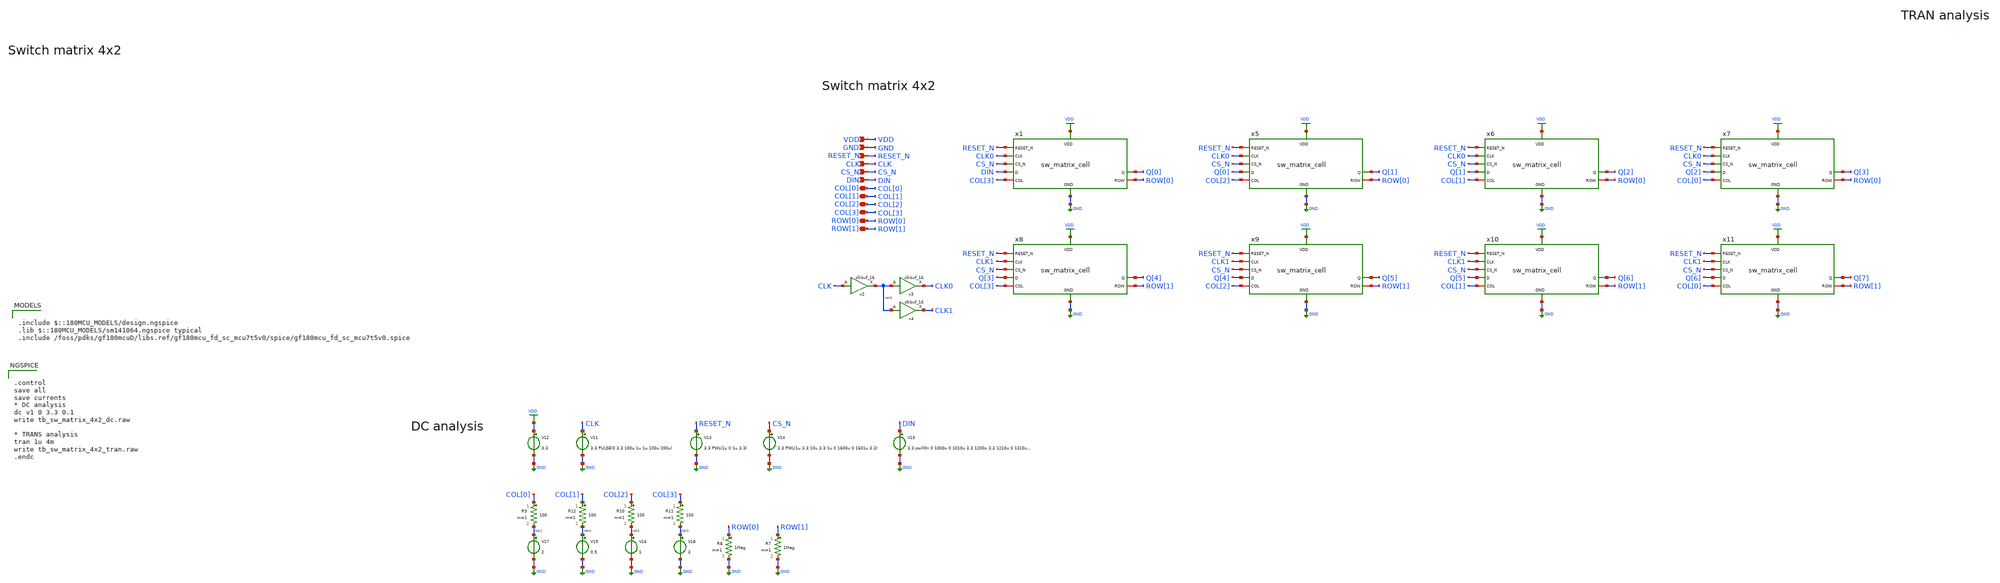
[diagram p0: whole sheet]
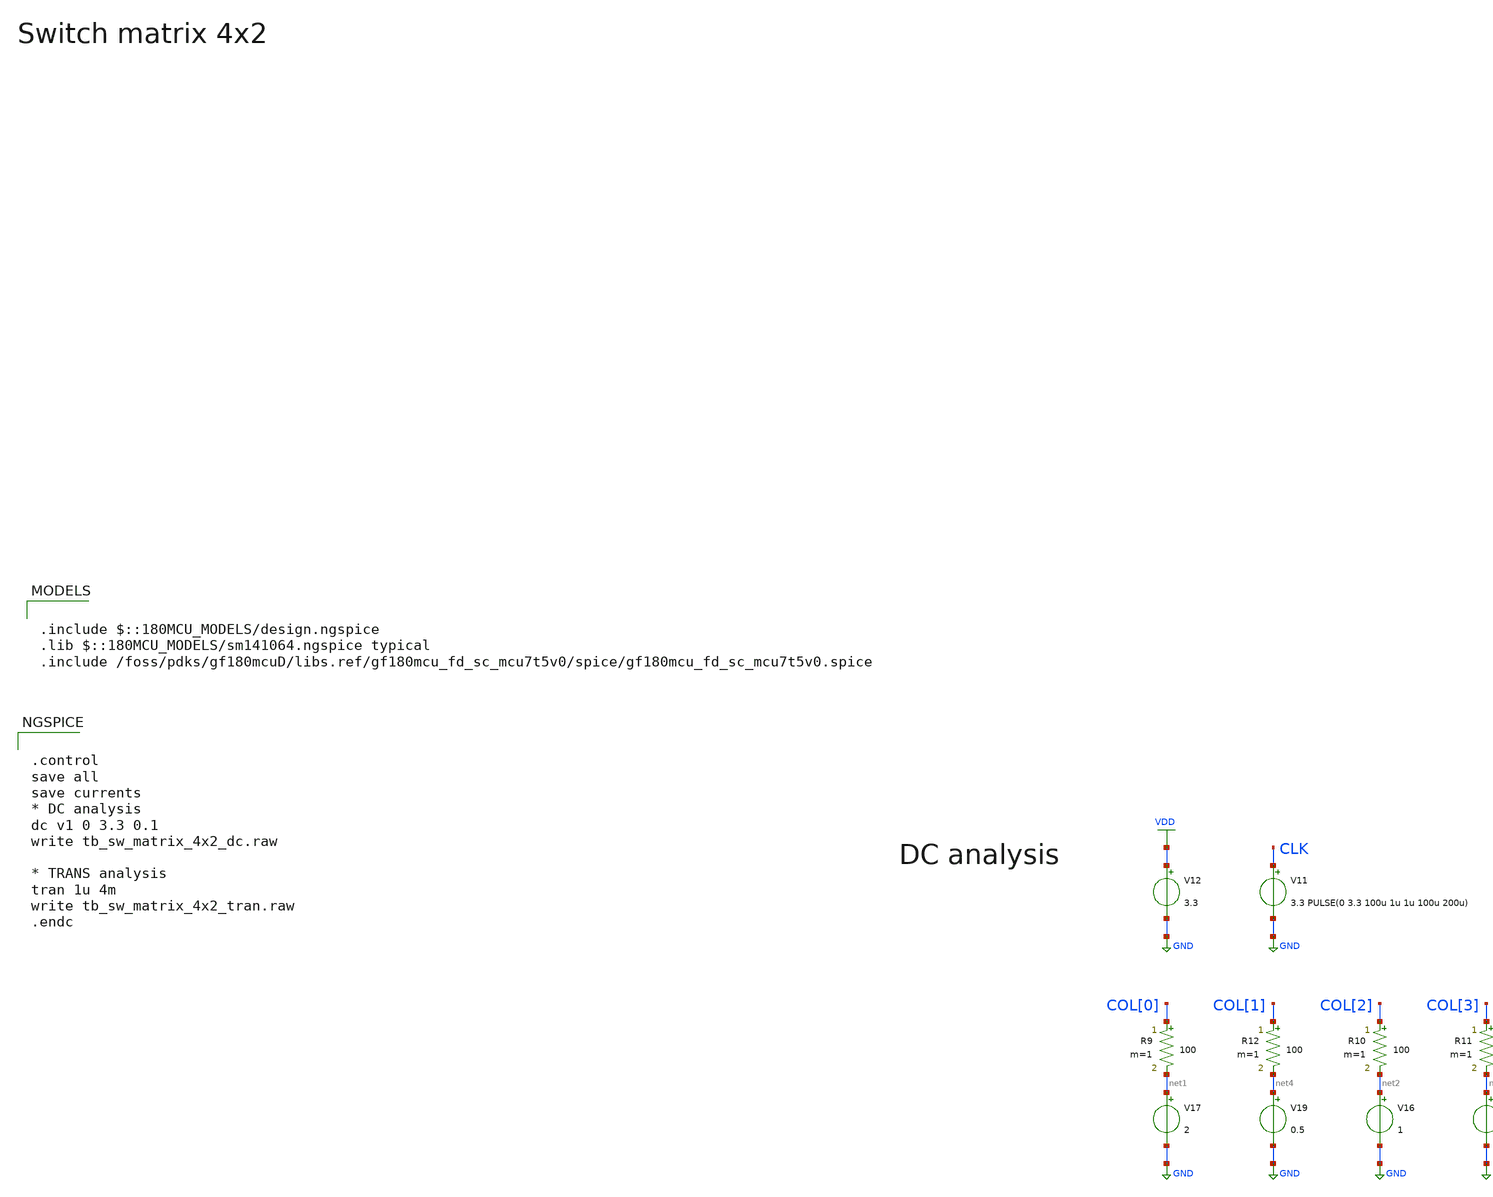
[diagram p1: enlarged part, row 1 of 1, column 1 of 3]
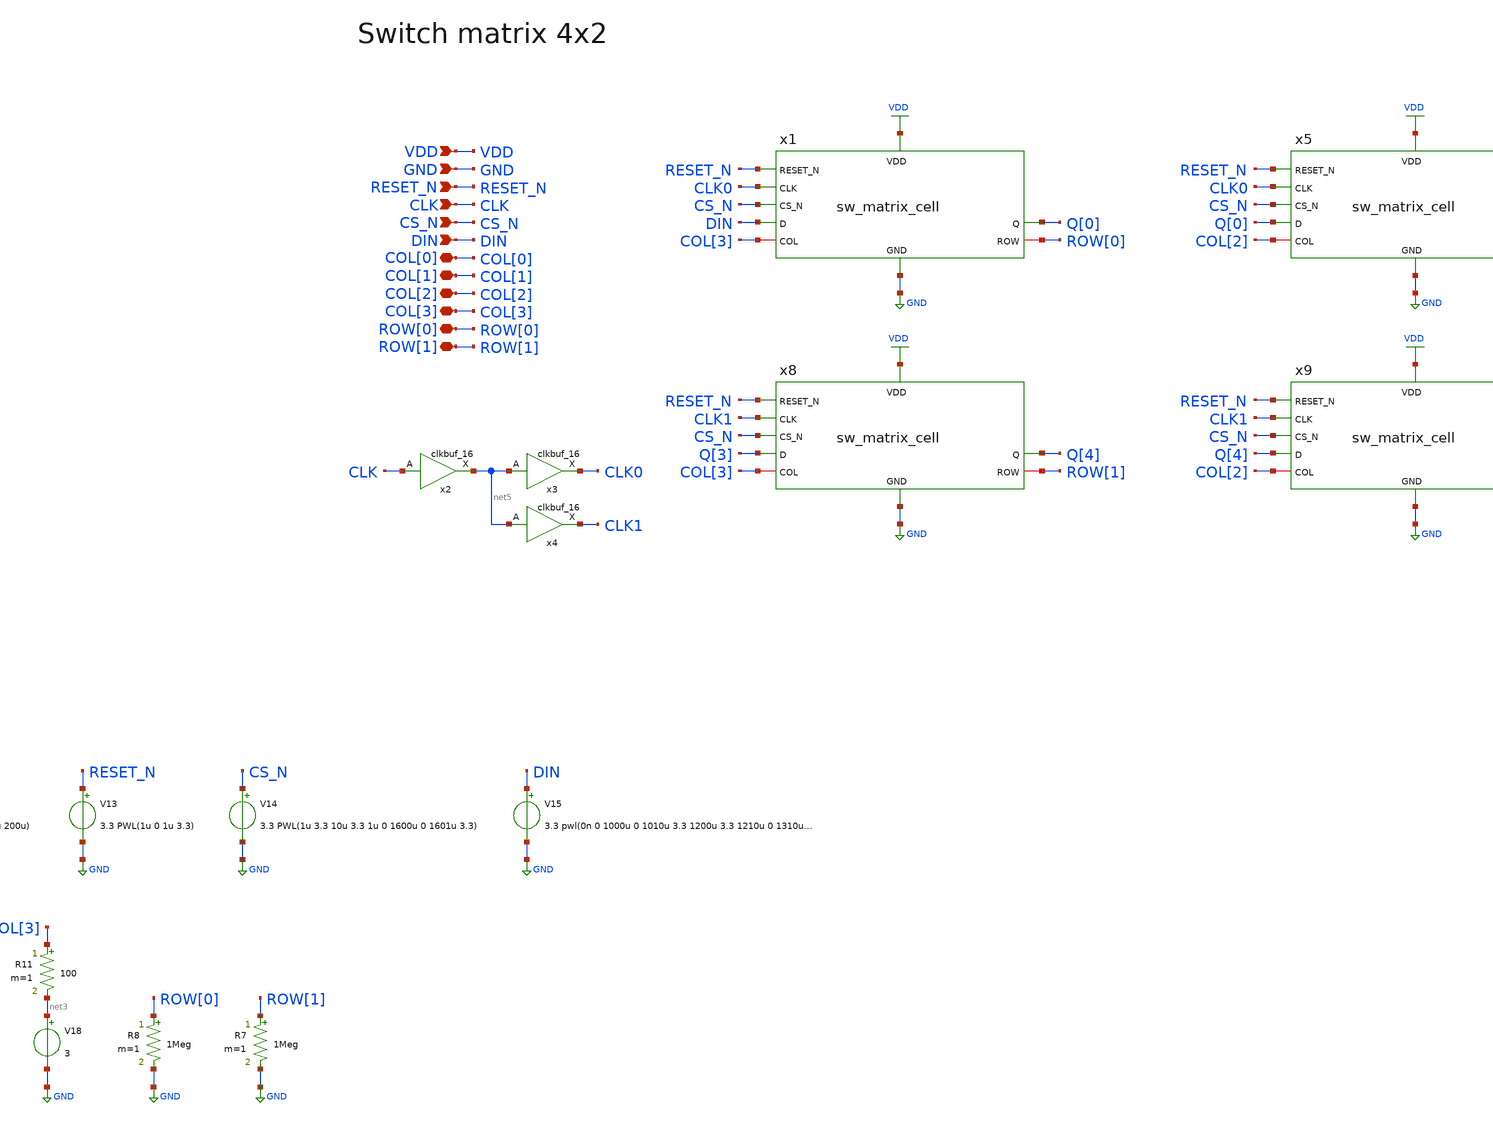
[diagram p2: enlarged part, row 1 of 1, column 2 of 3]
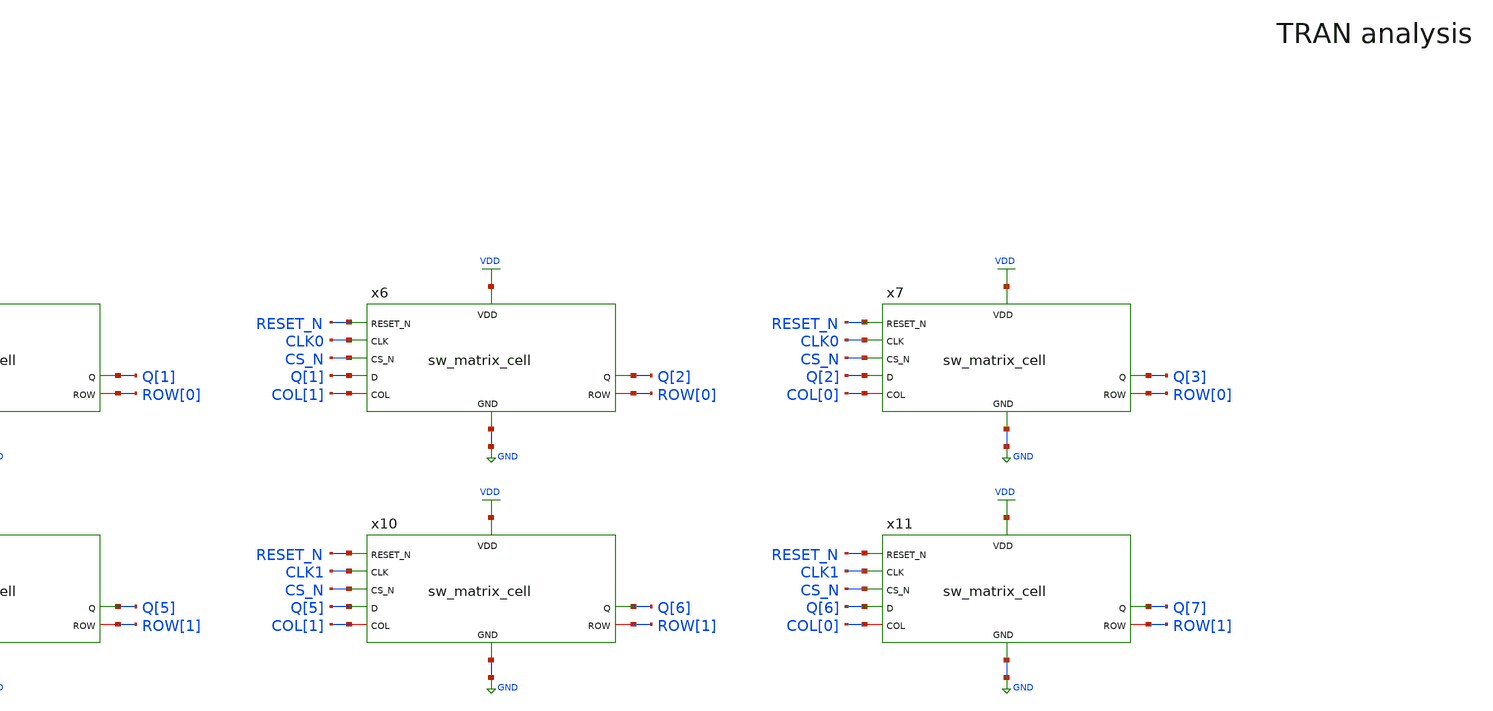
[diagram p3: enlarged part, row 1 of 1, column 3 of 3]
** sch_path: designs/libs/tb_analog/tb_sw_matrix/tb_sw_matrix_4x2.sch
* Copyright 2022 GlobalFoundries PDK Authors
* Licensed under the Apache License, Version 2.0 (the "License");
* you may not use this file except in compliance with the License.
* You may obtain a copy of the License at
* https://www.apache.org/licenses/LICENSE-2.0
* Unless required by applicable law or agreed to in writing, software
* distributed under the License is distributed on an "AS IS" BASIS,
* WITHOUT WARRANTIES OR CONDITIONS OF ANY KIND, either express or implied.
* See the License for the specific language governing permissions and
* limitations under the License.
**.subckt tb_sw_matrix_4x2 VDD GND RESET_N CLK CS_N DIN COL[0] COL[1] COL[2] COL[3] ROW[0] ROW[1]
*.ipin VDD
*.ipin GND
*.ipin RESET_N
*.ipin CLK
*.ipin CS_N
*.ipin DIN
*.iopin COL[0]
*.iopin COL[1]
*.iopin COL[2]
*.iopin COL[3]
*.iopin ROW[0]
*.iopin ROW[1]
V11 CLK GND 3.3 PULSE(0 3.3 100u 1u 1u 100u 200u)
V12 VDD GND 3.3
R7 ROW[1] GND 1Meg m=1
R8 ROW[0] GND 1Meg m=1
V13 RESET_N GND 3.3 PWL(1u 0 1u 3.3)
V14 CS_N GND 3.3 PWL(1u 3.3 10u 3.3 1u 0 1600u 0 1601u 3.3)
V15 DIN GND 3.3 pwl(0n 0 1000u 0 1010u 3.3 1200u 3.3 1210u 0 1310u 0)
R9 COL[0] net1 100 m=1
R10 COL[2] net2 100 m=1
V16 net2 GND 1
V17 net1 GND 2
R11 COL[3] net3 100 m=1
V18 net3 GND 3
R12 COL[1] net4 100 m=1
V19 net4 GND 0.5
x1 VDD GND RESET_N CLK0 DIN CS_N Q[0] COL[3] ROW[0] sw_matrix_cell
x5 VDD GND RESET_N CLK0 Q[0] CS_N Q[1] COL[2] ROW[0] sw_matrix_cell
x6 VDD GND RESET_N CLK0 Q[1] CS_N Q[2] COL[1] ROW[0] sw_matrix_cell
x7 VDD GND RESET_N CLK0 Q[2] CS_N Q[3] COL[0] ROW[0] sw_matrix_cell
x8 VDD GND RESET_N CLK1 Q[3] CS_N Q[4] COL[3] ROW[1] sw_matrix_cell
x9 VDD GND RESET_N CLK1 Q[4] CS_N Q[5] COL[2] ROW[1] sw_matrix_cell
x10 VDD GND RESET_N CLK1 Q[5] CS_N Q[6] COL[1] ROW[1] sw_matrix_cell
x11 VDD GND RESET_N CLK1 Q[6] CS_N Q[7] COL[0] ROW[1] sw_matrix_cell
x2 CLK net5 VDD VDD GND GND gf180mcu_fd_sc_mcu7t5v0__clkbuf_16
x3 net5 CLK0 VDD VDD GND GND gf180mcu_fd_sc_mcu7t5v0__clkbuf_16
x4 net5 CLK1 VDD VDD GND GND gf180mcu_fd_sc_mcu7t5v0__clkbuf_16
**** begin user architecture code

.include $::180MCU_MODELS/design.ngspice
.lib $::180MCU_MODELS/sm141064.ngspice typical
.include /foss/pdks/gf180mcuD/libs.ref/gf180mcu_fd_sc_mcu7t5v0/spice/gf180mcu_fd_sc_mcu7t5v0.spice



.control
save all
save currents
* DC analysis
dc v1 0 3.3 0.1
write tb_sw_matrix_4x2_dc.raw

* TRANS analysis
tran 1u 4m
write tb_sw_matrix_4x2_tran.raw
.endc


**** end user architecture code
**.ends
.GLOBAL GND
.GLOBAL VDD
.end
